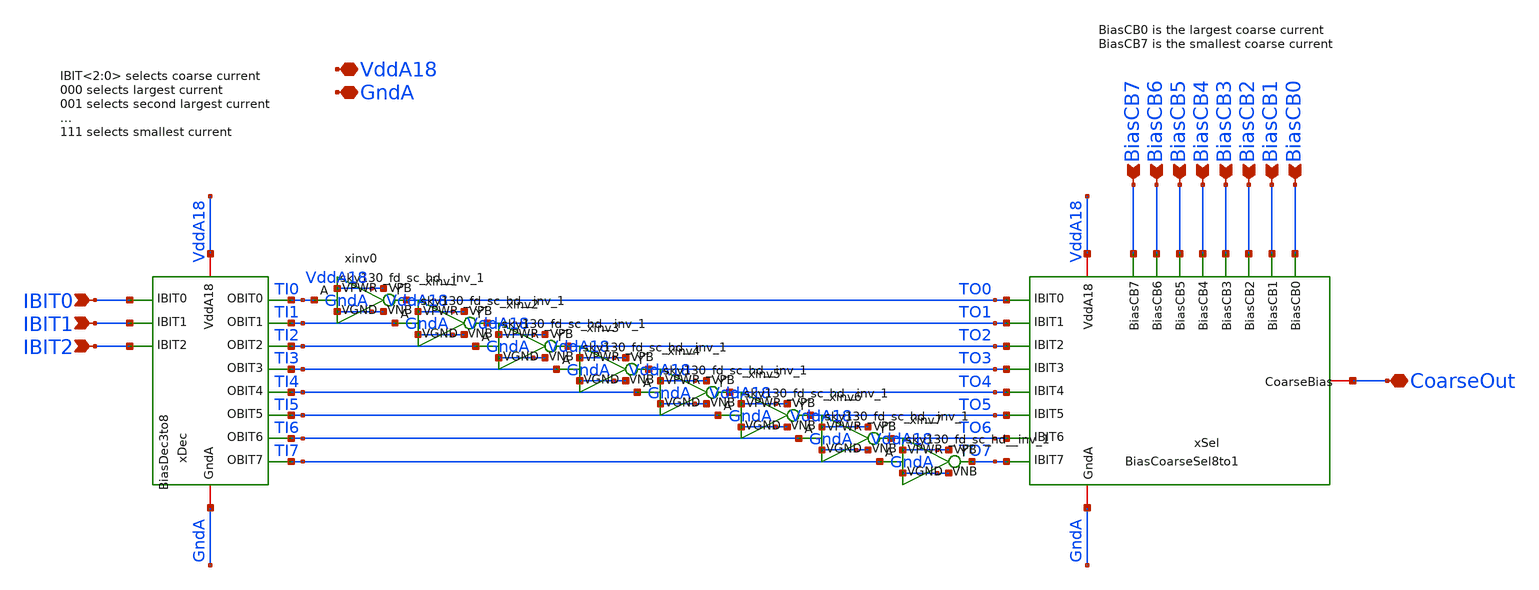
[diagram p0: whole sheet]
** sch_path: analog/xschem/BiasCoarseBuffer.sch
**.subckt BiasCoarseBuffer VddA18 GndA BiasCB7 BiasCB6 BiasCB5 BiasCB4 BiasCB3 BiasCB2 BiasCB1
*+ BiasCB0 IBIT0 IBIT1 IBIT2 CoarseOut
*.iopin VddA18
*.iopin GndA
*.ipin BiasCB7
*.ipin BiasCB6
*.ipin BiasCB5
*.ipin BiasCB4
*.ipin BiasCB3
*.ipin BiasCB2
*.ipin BiasCB1
*.ipin BiasCB0
*.ipin IBIT0
*.ipin IBIT1
*.ipin IBIT2
*.iopin CoarseOut
xSel VddA18 GndA TO0 TO1 TO3 TO4 TO5 TO6 TO7 TO2 BiasCB0 BiasCB1 BiasCB3 BiasCB4 BiasCB5 BiasCB6
+ BiasCB7 BiasCB2 CoarseOut BiasCoarseSel8to1
xDec VddA18 GndA TI0 TI1 TI3 TI4 TI5 TI6 TI7 TI2 IBIT0 IBIT1 IBIT2 BiasDec3to8
xinv0 TI0 TO0 VddA18 VddA18 GndA GndA sky130_fd_sc_hd__inv_1
xinv1 TI1 TO1 VddA18 VddA18 GndA GndA sky130_fd_sc_hd__inv_1
xinv2 TI2 TO2 VddA18 VddA18 GndA GndA sky130_fd_sc_hd__inv_1
xinv3 TI3 TO3 VddA18 VddA18 GndA GndA sky130_fd_sc_hd__inv_1
xinv4 TI4 TO4 VddA18 VddA18 GndA GndA sky130_fd_sc_hd__inv_1
xinv5 TI5 TO5 VddA18 VddA18 GndA GndA sky130_fd_sc_hd__inv_1
xinv6 TI6 TO6 VddA18 VddA18 GndA GndA sky130_fd_sc_hd__inv_1
xinv7 TI7 TO7 VddA18 VddA18 GndA GndA sky130_fd_sc_hd__inv_1
**.ends
.end
